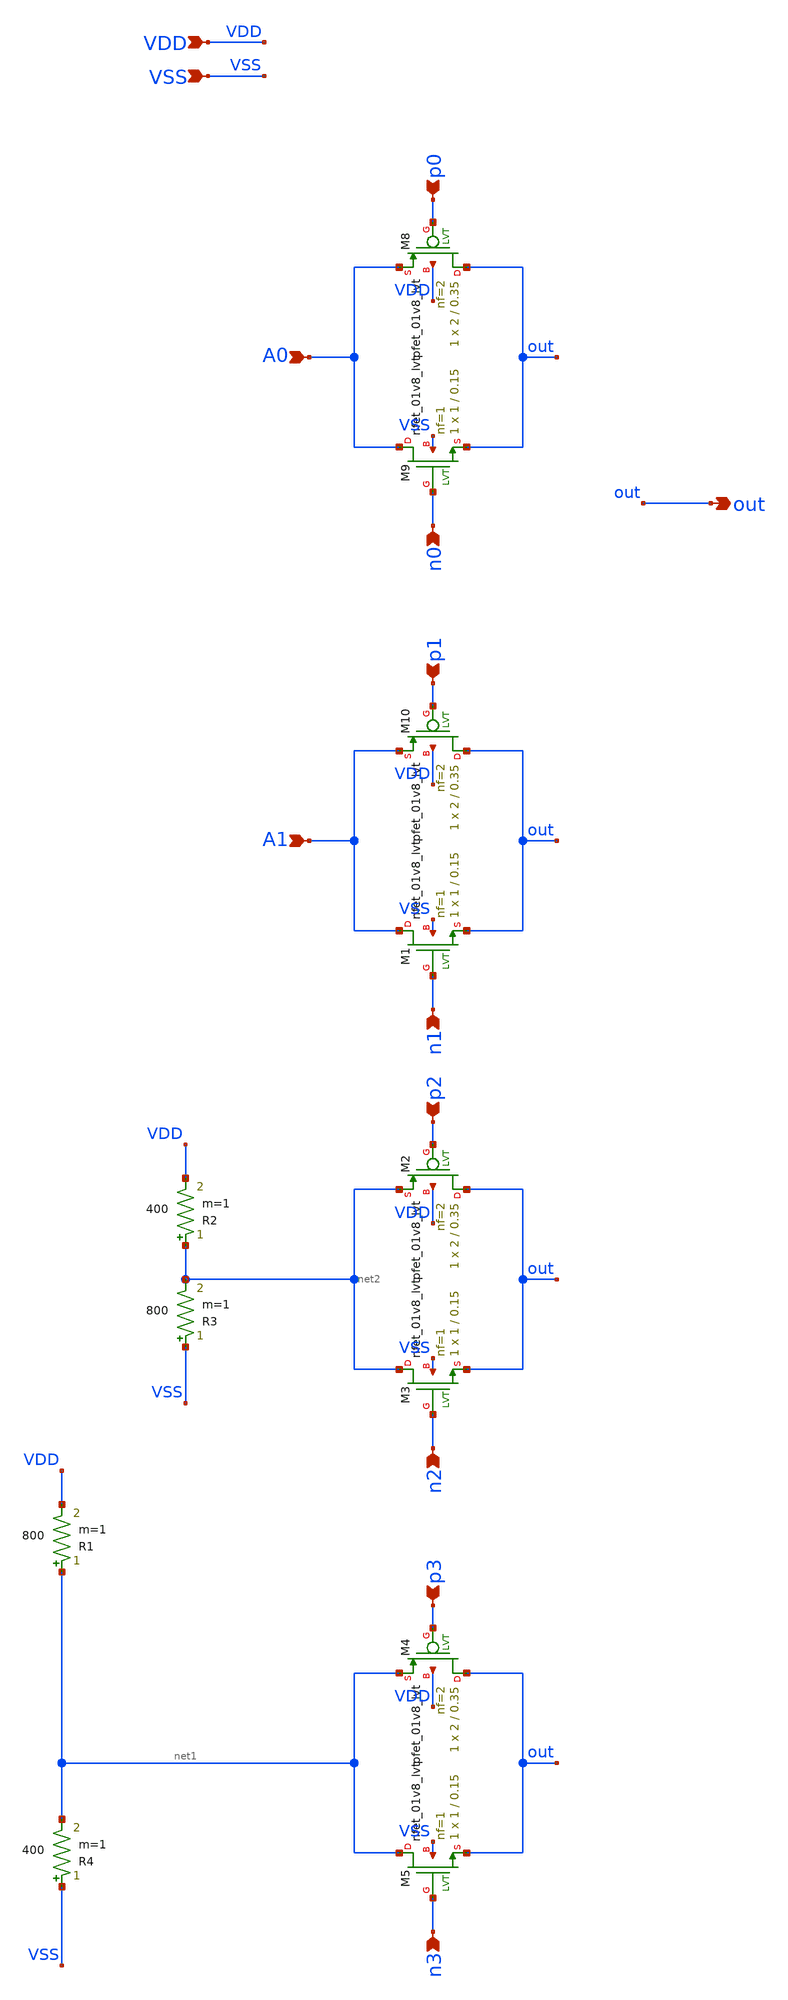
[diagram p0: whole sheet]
** sch_path: xschem/Mux.sch
**.subckt Mux VDD VSS p0 n0 A0 p1 n1 A1 p2 n2 p3 n3 out
*.ipin VDD
*.ipin VSS
*.ipin p0
*.ipin n0
*.ipin A0
*.ipin p1
*.ipin n1
*.ipin A1
*.ipin p2
*.ipin n2
*.ipin p3
*.ipin n3
*.opin out
R1 net1 VDD 800 m=1
XM8 out p0 A0 VDD sky130_fd_pr__pfet_01v8_lvt L=0.35 W=2 nf=2 ad='int((2 + 1)/2) * 2 / 2 * 0.29' as='int((2 + 2)/2) * 2 / 2 * 0.29'
+ pd='2*int((2 + 1)/2) * (2 / 2 + 0.29)' ps='2*int((2 + 2)/2) * (2 / 2 + 0.29)' nrd='0.29 / 2 ' nrs='0.29 / 2 '
+ sa=0 sb=0 sd=0 mult=1 m=1
XM9 A0 n0 out VSS sky130_fd_pr__nfet_01v8_lvt L=0.15 W=1 nf=1 ad='int((1 + 1)/2) * 1 / 1 * 0.29' as='int((1 + 2)/2) * 1 / 1 * 0.29'
+ pd='2*int((1 + 1)/2) * (1 / 1 + 0.29)' ps='2*int((1 + 2)/2) * (1 / 1 + 0.29)' nrd='0.29 / 1 ' nrs='0.29 / 1 '
+ sa=0 sb=0 sd=0 mult=1 m=1
XM10 out p1 A1 VDD sky130_fd_pr__pfet_01v8_lvt L=0.35 W=2 nf=2 ad='int((2 + 1)/2) * 2 / 2 * 0.29' as='int((2 + 2)/2) * 2 / 2 * 0.29'
+ pd='2*int((2 + 1)/2) * (2 / 2 + 0.29)' ps='2*int((2 + 2)/2) * (2 / 2 + 0.29)' nrd='0.29 / 2 ' nrs='0.29 / 2 '
+ sa=0 sb=0 sd=0 mult=1 m=1
XM1 A1 n1 out VSS sky130_fd_pr__nfet_01v8_lvt L=0.15 W=1 nf=1 ad='int((1 + 1)/2) * 1 / 1 * 0.29' as='int((1 + 2)/2) * 1 / 1 * 0.29'
+ pd='2*int((1 + 1)/2) * (1 / 1 + 0.29)' ps='2*int((1 + 2)/2) * (1 / 1 + 0.29)' nrd='0.29 / 1 ' nrs='0.29 / 1 '
+ sa=0 sb=0 sd=0 mult=1 m=1
XM2 out p2 net2 VDD sky130_fd_pr__pfet_01v8_lvt L=0.35 W=2 nf=2 ad='int((2 + 1)/2) * 2 / 2 * 0.29' as='int((2 + 2)/2) * 2 / 2 * 0.29'
+ pd='2*int((2 + 1)/2) * (2 / 2 + 0.29)' ps='2*int((2 + 2)/2) * (2 / 2 + 0.29)' nrd='0.29 / 2 ' nrs='0.29 / 2 '
+ sa=0 sb=0 sd=0 mult=1 m=1
XM3 net2 n2 out VSS sky130_fd_pr__nfet_01v8_lvt L=0.15 W=1 nf=1 ad='int((1 + 1)/2) * 1 / 1 * 0.29' as='int((1 + 2)/2) * 1 / 1 * 0.29'
+ pd='2*int((1 + 1)/2) * (1 / 1 + 0.29)' ps='2*int((1 + 2)/2) * (1 / 1 + 0.29)' nrd='0.29 / 1 ' nrs='0.29 / 1 '
+ sa=0 sb=0 sd=0 mult=1 m=1
XM4 out p3 net1 VDD sky130_fd_pr__pfet_01v8_lvt L=0.35 W=2 nf=2 ad='int((2 + 1)/2) * 2 / 2 * 0.29' as='int((2 + 2)/2) * 2 / 2 * 0.29'
+ pd='2*int((2 + 1)/2) * (2 / 2 + 0.29)' ps='2*int((2 + 2)/2) * (2 / 2 + 0.29)' nrd='0.29 / 2 ' nrs='0.29 / 2 '
+ sa=0 sb=0 sd=0 mult=1 m=1
XM5 net1 n3 out VSS sky130_fd_pr__nfet_01v8_lvt L=0.15 W=1 nf=1 ad='int((1 + 1)/2) * 1 / 1 * 0.29' as='int((1 + 2)/2) * 1 / 1 * 0.29'
+ pd='2*int((1 + 1)/2) * (1 / 1 + 0.29)' ps='2*int((1 + 2)/2) * (1 / 1 + 0.29)' nrd='0.29 / 1 ' nrs='0.29 / 1 '
+ sa=0 sb=0 sd=0 mult=1 m=1
R2 net2 VDD 400 m=1
R3 VSS net2 800 m=1
R4 VSS net1 400 m=1
**.ends
.end
